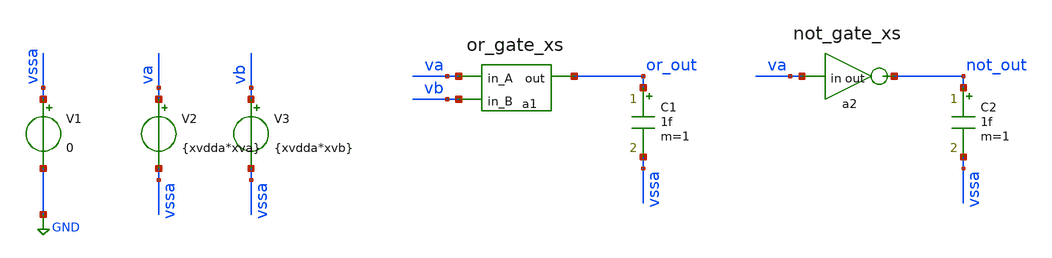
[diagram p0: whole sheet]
** sch_path: Running_xspice_models/tb_xspice.sch
**.subckt tb_xspice
V1 vssa GND 0
V2 va vssa {xvdda*xva}
V3 vb vssa {xvdda*xvb}
C1 or_out vssa 1f m=1
a1 [ va vb ] or_out or_gate_xs
a2 va not_out not_gate_xs
C2 not_out vssa 1f m=1
**** begin user architecture code

** opencircuitdesign pdks install
.lib /home/slice/pdk/iHP/IHP-Open-PDK/ihp-sg13g2/libs.tech/ngspice/models/cornerMOSlv.lib mos_tt
*.include ${PDK_ROOT}/${PDK}/libs.ref/sg13g2_stdcell/spice/sg13g2_stdcell.spice
.include /home/slice/pdk/iHP/IHP-Open-PDK/ihp-sg13g2/libs.ref/sg13g2_stdcell/spice/sg13g2_stdcell.spice

* Parameters
.param xvdda = 1.8
.param xva = 0
.param xvb = 1
.param xtsim = 5u
.csparam xtsim_var = 'xtsim'
.param xtstep = 1n
.csparam xtstep_var = 'xtstep'

.save v(va) v(vb) v(or_out) v(not_out)

.model or_gate_xs d_or(rise_delay = 0.5e-9 fall_delay = 0.3e-9  input_load = 0.5e-12)

.model not_gate_xs d_inverter(rise_delay = 0.5e-9 fall_delay = 0.3e-9  input_load = 0.5e-12)

.model auto_dac dac_bridge(out_low = 0 out_high = 1.8 t_rise = 10p t_fall = 10p)

  .control

** TRAN ANALYSIS **

 tran $&xtstep_var $&xtsim_var
  *set filetype=ascii
  remzerovec
  write tb_xspice.raw

    plot tran.v(or_out) tran.v(va) tran.v(vb)

  setplot
  listing e
*quit 0
.endc




**** end user architecture code
**.ends

* expanding   symbol:  or_gate_xs.sym # of pins=3
** sym_path: Running_xspice_models/or_gate_xs.sym
** sch_path: Running_xspice_models/or_gate_xs.sch
.subckt or_gate_xs in_A in_B out
*.ipin in_A
*.ipin in_B
*.opin out
* noconn out
* noconn in_A
* noconn in_B
**** begin user architecture code
Agate [in_A in_B] out or_gate_xs
**** end user architecture code
.ends


* expanding   symbol:  not_gate_xs.sym # of pins=2
** sym_path: Running_xspice_models/not_gate_xs.sym
** sch_path: Running_xspice_models/not_gate_xs.sch
.subckt not_gate_xs in out
*.ipin in
*.opin out
* noconn out
* noconn in
**** begin user architecture code
Agate in out not_gate_xs
**** end user architecture code
.ends

.GLOBAL GND
.end
